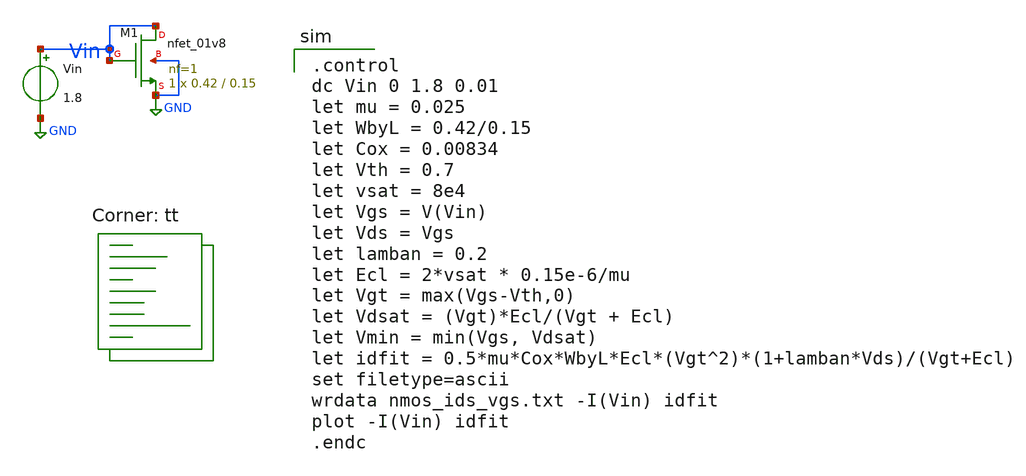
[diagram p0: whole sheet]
** sch_path: tutorial_2/tutorial_2_1a.sch
**.subckt tutorial_2_1a
XM1 Vin Vin GND GND sky130_fd_pr__nfet_01v8 L=0.15 W=0.42 nf=1 ad='int((nf+1)/2) * W/nf * 0.29' as='int((nf+2)/2) * W/nf * 0.29'
+ pd='2*int((nf+1)/2) * (W/nf + 0.29)' ps='2*int((nf+2)/2) * (W/nf + 0.29)' nrd='0.29 / W' nrs='0.29 / W'
+ sa=0 sb=0 sd=0 mult=1 m=1
Vin Vin GND 1.8
**** begin user architecture code

.control
dc Vin 0 1.8 0.01
let mu = 0.025
let WbyL = 0.42/0.15
let Cox = 0.00834
let Vth = 0.7
let vsat = 8e4
let Vgs = V(Vin)
let Vds = Vgs
let lamban = 0.2
let Ecl = 2*vsat * 0.15e-6/mu
let Vgt = max(Vgs-Vth,0)
let Vdsat = (Vgt)*Ecl/(Vgt + Ecl)
let Vmin = min(Vgs, Vdsat)
let idfit = 0.5*mu*Cox*WbyL*Ecl*(Vgt^2)*(1+lamban*Vds)/(Vgt+Ecl)
set filetype=ascii
wrdata nmos_ids_vgs.txt -I(Vin) idfit
plot -I(Vin) idfit
.endc

.lib $::SKYWATER_MODELS/sky130.lib.spice tt
**** end user architecture code
**.ends
.GLOBAL GND
.end
